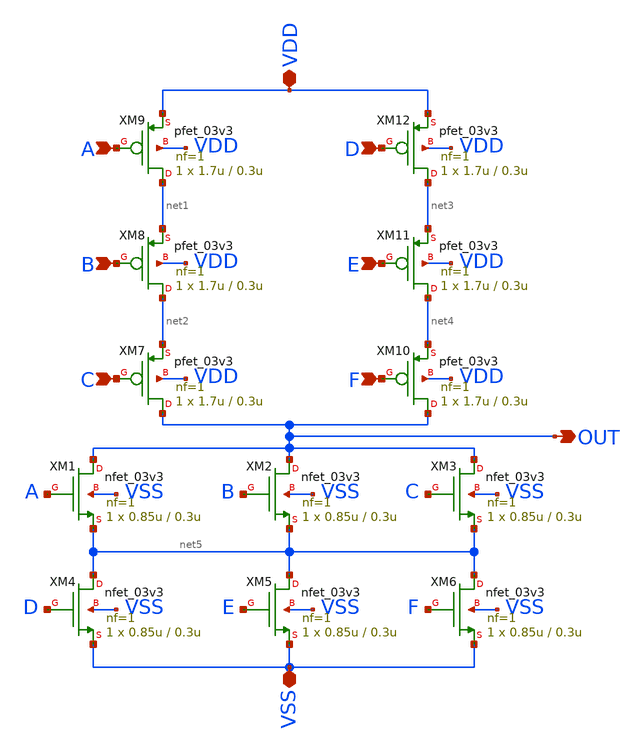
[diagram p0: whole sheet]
** sch_path: designs/OAI33/xschem/OAI33.sch
**.subckt OAI33 VDD VSS A OUT B C F D E
*.iopin VDD
*.iopin VSS
*.ipin A
*.opin OUT
*.ipin B
*.ipin C
*.ipin F
*.ipin D
*.ipin E
XM1 OUT A net5 VSS nfet_03v3 L=0.3u W=0.85u nf=1 ad='int((nf+1)/2) * W/nf * 0.18u' as='int((nf+2)/2) * W/nf * 0.18u'
+ pd='2*int((nf+1)/2) * (W/nf + 0.18u)' ps='2*int((nf+2)/2) * (W/nf + 0.18u)' nrd='0.18u / W' nrs='0.18u / W'
+ sa=0 sb=0 sd=0 m=1
XM7 OUT C net2 VDD pfet_03v3 L=0.3u W=1.7u nf=1 ad='int((nf+1)/2) * W/nf * 0.18u' as='int((nf+2)/2) * W/nf * 0.18u'
+ pd='2*int((nf+1)/2) * (W/nf + 0.18u)' ps='2*int((nf+2)/2) * (W/nf + 0.18u)' nrd='0.18u / W' nrs='0.18u / W'
+ sa=0 sb=0 sd=0 m=1
XM2 OUT B net5 VSS nfet_03v3 L=0.3u W=0.85u nf=1 ad='int((nf+1)/2) * W/nf * 0.18u' as='int((nf+2)/2) * W/nf * 0.18u'
+ pd='2*int((nf+1)/2) * (W/nf + 0.18u)' ps='2*int((nf+2)/2) * (W/nf + 0.18u)' nrd='0.18u / W' nrs='0.18u / W'
+ sa=0 sb=0 sd=0 m=1
XM3 OUT C net5 VSS nfet_03v3 L=0.3u W=0.85u nf=1 ad='int((nf+1)/2) * W/nf * 0.18u' as='int((nf+2)/2) * W/nf * 0.18u'
+ pd='2*int((nf+1)/2) * (W/nf + 0.18u)' ps='2*int((nf+2)/2) * (W/nf + 0.18u)' nrd='0.18u / W' nrs='0.18u / W'
+ sa=0 sb=0 sd=0 m=1
XM4 net5 D VSS VSS nfet_03v3 L=0.3u W=0.85u nf=1 ad='int((nf+1)/2) * W/nf * 0.18u' as='int((nf+2)/2) * W/nf * 0.18u'
+ pd='2*int((nf+1)/2) * (W/nf + 0.18u)' ps='2*int((nf+2)/2) * (W/nf + 0.18u)' nrd='0.18u / W' nrs='0.18u / W'
+ sa=0 sb=0 sd=0 m=1
XM5 net5 E VSS VSS nfet_03v3 L=0.3u W=0.85u nf=1 ad='int((nf+1)/2) * W/nf * 0.18u' as='int((nf+2)/2) * W/nf * 0.18u'
+ pd='2*int((nf+1)/2) * (W/nf + 0.18u)' ps='2*int((nf+2)/2) * (W/nf + 0.18u)' nrd='0.18u / W' nrs='0.18u / W'
+ sa=0 sb=0 sd=0 m=1
XM6 net5 F VSS VSS nfet_03v3 L=0.3u W=0.85u nf=1 ad='int((nf+1)/2) * W/nf * 0.18u' as='int((nf+2)/2) * W/nf * 0.18u'
+ pd='2*int((nf+1)/2) * (W/nf + 0.18u)' ps='2*int((nf+2)/2) * (W/nf + 0.18u)' nrd='0.18u / W' nrs='0.18u / W'
+ sa=0 sb=0 sd=0 m=1
XM8 net2 B net1 VDD pfet_03v3 L=0.3u W=1.7u nf=1 ad='int((nf+1)/2) * W/nf * 0.18u' as='int((nf+2)/2) * W/nf * 0.18u'
+ pd='2*int((nf+1)/2) * (W/nf + 0.18u)' ps='2*int((nf+2)/2) * (W/nf + 0.18u)' nrd='0.18u / W' nrs='0.18u / W'
+ sa=0 sb=0 sd=0 m=1
XM9 net1 A VDD VDD pfet_03v3 L=0.3u W=1.7u nf=1 ad='int((nf+1)/2) * W/nf * 0.18u' as='int((nf+2)/2) * W/nf * 0.18u'
+ pd='2*int((nf+1)/2) * (W/nf + 0.18u)' ps='2*int((nf+2)/2) * (W/nf + 0.18u)' nrd='0.18u / W' nrs='0.18u / W'
+ sa=0 sb=0 sd=0 m=1
XM10 OUT F net4 VDD pfet_03v3 L=0.3u W=1.7u nf=1 ad='int((nf+1)/2) * W/nf * 0.18u' as='int((nf+2)/2) * W/nf * 0.18u'
+ pd='2*int((nf+1)/2) * (W/nf + 0.18u)' ps='2*int((nf+2)/2) * (W/nf + 0.18u)' nrd='0.18u / W' nrs='0.18u / W'
+ sa=0 sb=0 sd=0 m=1
XM11 net4 E net3 VDD pfet_03v3 L=0.3u W=1.7u nf=1 ad='int((nf+1)/2) * W/nf * 0.18u' as='int((nf+2)/2) * W/nf * 0.18u'
+ pd='2*int((nf+1)/2) * (W/nf + 0.18u)' ps='2*int((nf+2)/2) * (W/nf + 0.18u)' nrd='0.18u / W' nrs='0.18u / W'
+ sa=0 sb=0 sd=0 m=1
XM12 net3 D VDD VDD pfet_03v3 L=0.3u W=1.7u nf=1 ad='int((nf+1)/2) * W/nf * 0.18u' as='int((nf+2)/2) * W/nf * 0.18u'
+ pd='2*int((nf+1)/2) * (W/nf + 0.18u)' ps='2*int((nf+2)/2) * (W/nf + 0.18u)' nrd='0.18u / W' nrs='0.18u / W'
+ sa=0 sb=0 sd=0 m=1
**.ends
.end
